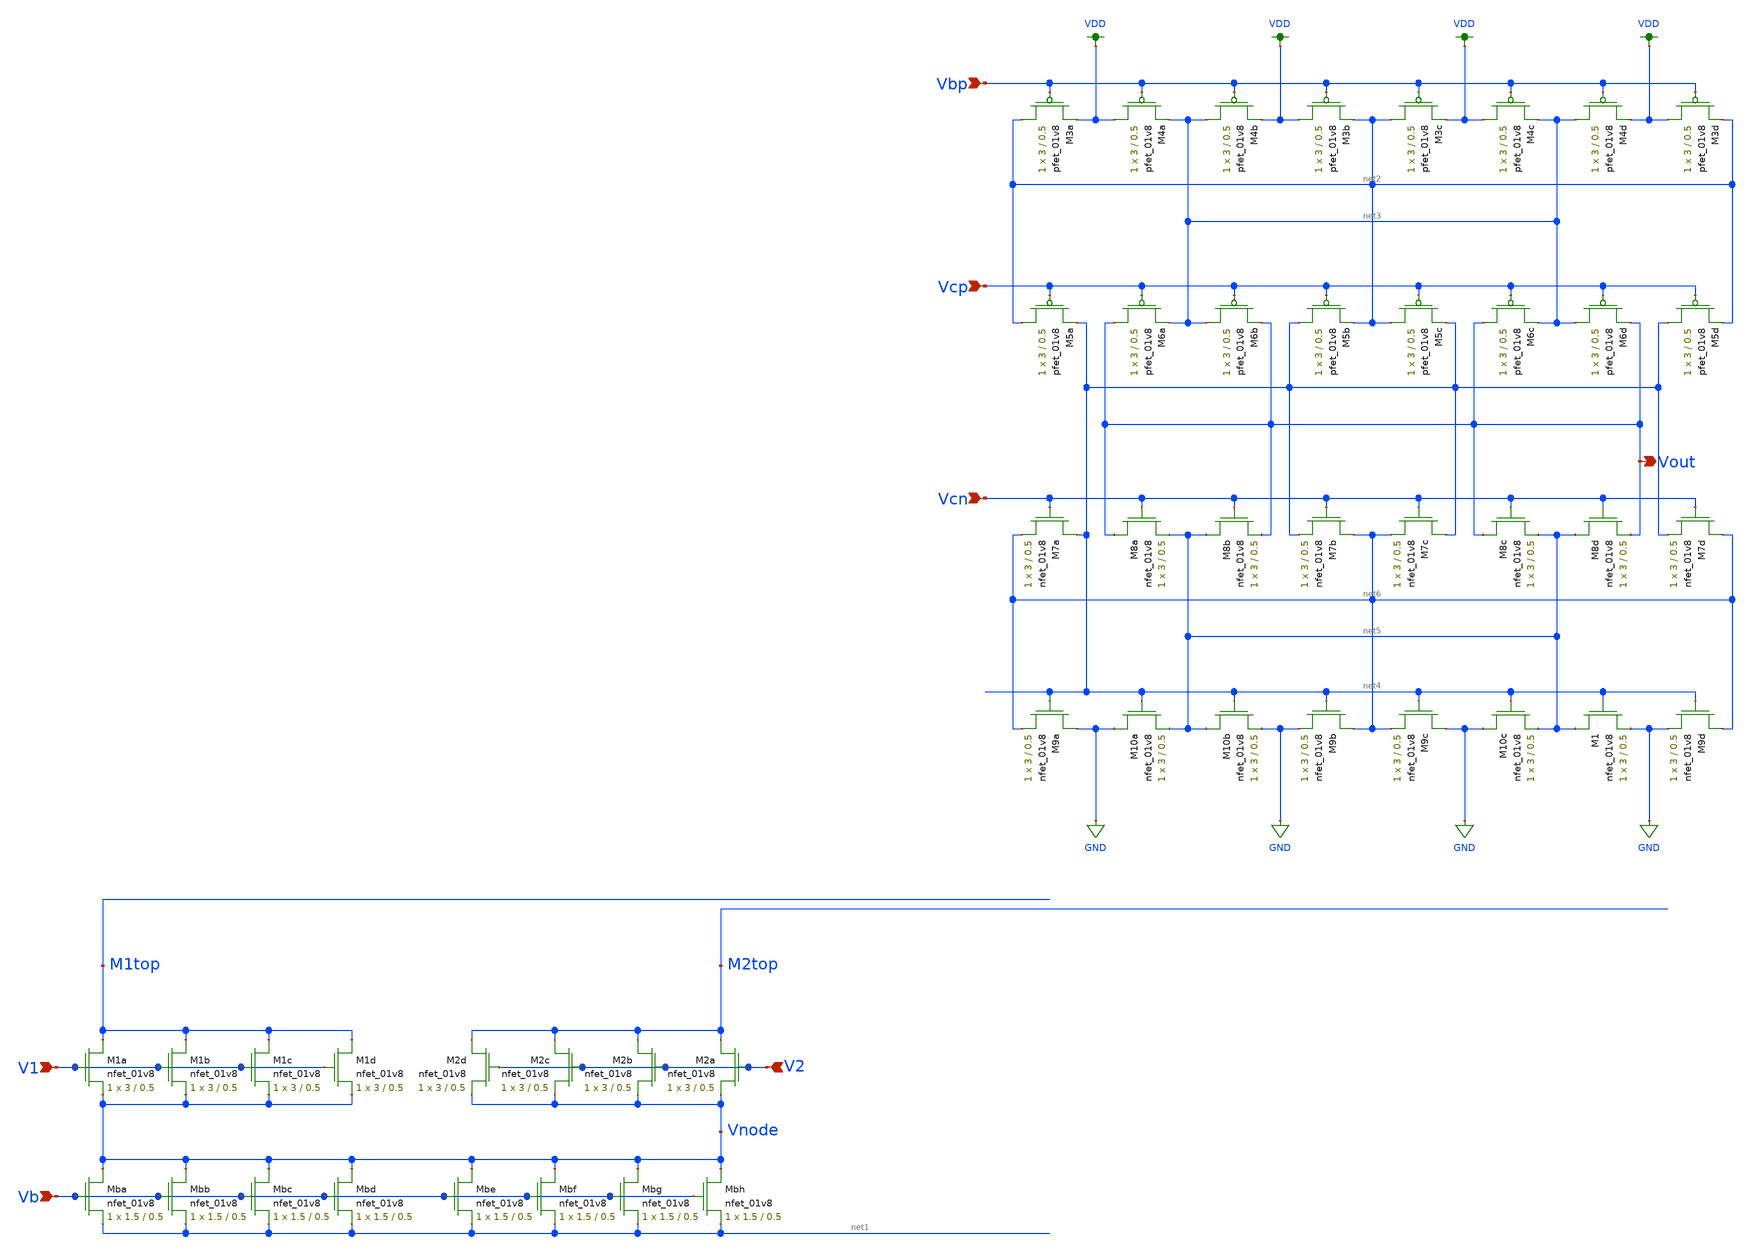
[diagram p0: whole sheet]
** sch_path: mp3/xschem/opamp_layout.sch
**.subckt opamp_layout Vbp Vcp Vcn V2 V1 Vb Vout
*.ipin Vbp
*.ipin Vcp
*.ipin Vcn
*.ipin V2
*.ipin V1
*.ipin Vb
*.opin Vout
XM1a M1top V1 Vnode GND sky130_fd_pr__nfet_01v8 L=0.5 W=3 nf=1 ad='int((nf+1)/2) * W/nf * 0.29' as='int((nf+2)/2) * W/nf * 0.29'
+ pd='2*int((nf+1)/2) * (W/nf + 0.29)' ps='2*int((nf+2)/2) * (W/nf + 0.29)' nrd='0.29 / W' nrs='0.29 / W'
+ sa=0 sb=0 sd=0 mult=1 m=1
XM1b M1top V1 Vnode GND sky130_fd_pr__nfet_01v8 L=0.5 W=3 nf=1 ad='int((nf+1)/2) * W/nf * 0.29' as='int((nf+2)/2) * W/nf * 0.29'
+ pd='2*int((nf+1)/2) * (W/nf + 0.29)' ps='2*int((nf+2)/2) * (W/nf + 0.29)' nrd='0.29 / W' nrs='0.29 / W'
+ sa=0 sb=0 sd=0 mult=1 m=1
XM1c M1top V1 Vnode GND sky130_fd_pr__nfet_01v8 L=0.5 W=3 nf=1 ad='int((nf+1)/2) * W/nf * 0.29' as='int((nf+2)/2) * W/nf * 0.29'
+ pd='2*int((nf+1)/2) * (W/nf + 0.29)' ps='2*int((nf+2)/2) * (W/nf + 0.29)' nrd='0.29 / W' nrs='0.29 / W'
+ sa=0 sb=0 sd=0 mult=1 m=1
XM1d M1top V1 Vnode GND sky130_fd_pr__nfet_01v8 L=0.5 W=3 nf=1 ad='int((nf+1)/2) * W/nf * 0.29' as='int((nf+2)/2) * W/nf * 0.29'
+ pd='2*int((nf+1)/2) * (W/nf + 0.29)' ps='2*int((nf+2)/2) * (W/nf + 0.29)' nrd='0.29 / W' nrs='0.29 / W'
+ sa=0 sb=0 sd=0 mult=1 m=1
XM2a M2top V2 Vnode GND sky130_fd_pr__nfet_01v8 L=0.5 W=3 nf=1 ad='int((nf+1)/2) * W/nf * 0.29' as='int((nf+2)/2) * W/nf * 0.29'
+ pd='2*int((nf+1)/2) * (W/nf + 0.29)' ps='2*int((nf+2)/2) * (W/nf + 0.29)' nrd='0.29 / W' nrs='0.29 / W'
+ sa=0 sb=0 sd=0 mult=1 m=1
XM2b M2top V2 Vnode GND sky130_fd_pr__nfet_01v8 L=0.5 W=3 nf=1 ad='int((nf+1)/2) * W/nf * 0.29' as='int((nf+2)/2) * W/nf * 0.29'
+ pd='2*int((nf+1)/2) * (W/nf + 0.29)' ps='2*int((nf+2)/2) * (W/nf + 0.29)' nrd='0.29 / W' nrs='0.29 / W'
+ sa=0 sb=0 sd=0 mult=1 m=1
XM2c M2top V2 Vnode GND sky130_fd_pr__nfet_01v8 L=0.5 W=3 nf=1 ad='int((nf+1)/2) * W/nf * 0.29' as='int((nf+2)/2) * W/nf * 0.29'
+ pd='2*int((nf+1)/2) * (W/nf + 0.29)' ps='2*int((nf+2)/2) * (W/nf + 0.29)' nrd='0.29 / W' nrs='0.29 / W'
+ sa=0 sb=0 sd=0 mult=1 m=1
XM2d M2top V2 Vnode GND sky130_fd_pr__nfet_01v8 L=0.5 W=3 nf=1 ad='int((nf+1)/2) * W/nf * 0.29' as='int((nf+2)/2) * W/nf * 0.29'
+ pd='2*int((nf+1)/2) * (W/nf + 0.29)' ps='2*int((nf+2)/2) * (W/nf + 0.29)' nrd='0.29 / W' nrs='0.29 / W'
+ sa=0 sb=0 sd=0 mult=1 m=1
XMba Vnode Vb net1 GND sky130_fd_pr__nfet_01v8 L=0.5 W=1.5 nf=1 ad='int((nf+1)/2) * W/nf * 0.29' as='int((nf+2)/2) * W/nf * 0.29'
+ pd='2*int((nf+1)/2) * (W/nf + 0.29)' ps='2*int((nf+2)/2) * (W/nf + 0.29)' nrd='0.29 / W' nrs='0.29 / W'
+ sa=0 sb=0 sd=0 mult=1 m=1
XMbb Vnode Vb net1 GND sky130_fd_pr__nfet_01v8 L=0.5 W=1.5 nf=1 ad='int((nf+1)/2) * W/nf * 0.29' as='int((nf+2)/2) * W/nf * 0.29'
+ pd='2*int((nf+1)/2) * (W/nf + 0.29)' ps='2*int((nf+2)/2) * (W/nf + 0.29)' nrd='0.29 / W' nrs='0.29 / W'
+ sa=0 sb=0 sd=0 mult=1 m=1
XMbc Vnode Vb net1 GND sky130_fd_pr__nfet_01v8 L=0.5 W=1.5 nf=1 ad='int((nf+1)/2) * W/nf * 0.29' as='int((nf+2)/2) * W/nf * 0.29'
+ pd='2*int((nf+1)/2) * (W/nf + 0.29)' ps='2*int((nf+2)/2) * (W/nf + 0.29)' nrd='0.29 / W' nrs='0.29 / W'
+ sa=0 sb=0 sd=0 mult=1 m=1
XMbd Vnode Vb net1 GND sky130_fd_pr__nfet_01v8 L=0.5 W=1.5 nf=1 ad='int((nf+1)/2) * W/nf * 0.29' as='int((nf+2)/2) * W/nf * 0.29'
+ pd='2*int((nf+1)/2) * (W/nf + 0.29)' ps='2*int((nf+2)/2) * (W/nf + 0.29)' nrd='0.29 / W' nrs='0.29 / W'
+ sa=0 sb=0 sd=0 mult=1 m=1
XMbe Vnode Vb net1 GND sky130_fd_pr__nfet_01v8 L=0.5 W=1.5 nf=1 ad='int((nf+1)/2) * W/nf * 0.29' as='int((nf+2)/2) * W/nf * 0.29'
+ pd='2*int((nf+1)/2) * (W/nf + 0.29)' ps='2*int((nf+2)/2) * (W/nf + 0.29)' nrd='0.29 / W' nrs='0.29 / W'
+ sa=0 sb=0 sd=0 mult=1 m=1
XMbf Vnode Vb net1 GND sky130_fd_pr__nfet_01v8 L=0.5 W=1.5 nf=1 ad='int((nf+1)/2) * W/nf * 0.29' as='int((nf+2)/2) * W/nf * 0.29'
+ pd='2*int((nf+1)/2) * (W/nf + 0.29)' ps='2*int((nf+2)/2) * (W/nf + 0.29)' nrd='0.29 / W' nrs='0.29 / W'
+ sa=0 sb=0 sd=0 mult=1 m=1
XMbg Vnode Vb net1 GND sky130_fd_pr__nfet_01v8 L=0.5 W=1.5 nf=1 ad='int((nf+1)/2) * W/nf * 0.29' as='int((nf+2)/2) * W/nf * 0.29'
+ pd='2*int((nf+1)/2) * (W/nf + 0.29)' ps='2*int((nf+2)/2) * (W/nf + 0.29)' nrd='0.29 / W' nrs='0.29 / W'
+ sa=0 sb=0 sd=0 mult=1 m=1
XMbh Vnode Vb net1 GND sky130_fd_pr__nfet_01v8 L=0.5 W=1.5 nf=1 ad='int((nf+1)/2) * W/nf * 0.29' as='int((nf+2)/2) * W/nf * 0.29'
+ pd='2*int((nf+1)/2) * (W/nf + 0.29)' ps='2*int((nf+2)/2) * (W/nf + 0.29)' nrd='0.29 / W' nrs='0.29 / W'
+ sa=0 sb=0 sd=0 mult=1 m=1
XM7a net4 Vcn net6 GND sky130_fd_pr__nfet_01v8 L=0.5 W=3 nf=1 ad='int((nf+1)/2) * W/nf * 0.29' as='int((nf+2)/2) * W/nf * 0.29'
+ pd='2*int((nf+1)/2) * (W/nf + 0.29)' ps='2*int((nf+2)/2) * (W/nf + 0.29)' nrd='0.29 / W' nrs='0.29 / W'
+ sa=0 sb=0 sd=0 mult=1 m=1
XM7b net6 Vcn net4 GND sky130_fd_pr__nfet_01v8 L=0.5 W=3 nf=1 ad='int((nf+1)/2) * W/nf * 0.29' as='int((nf+2)/2) * W/nf * 0.29'
+ pd='2*int((nf+1)/2) * (W/nf + 0.29)' ps='2*int((nf+2)/2) * (W/nf + 0.29)' nrd='0.29 / W' nrs='0.29 / W'
+ sa=0 sb=0 sd=0 mult=1 m=1
XM7c net4 Vcn net6 GND sky130_fd_pr__nfet_01v8 L=0.5 W=3 nf=1 ad='int((nf+1)/2) * W/nf * 0.29' as='int((nf+2)/2) * W/nf * 0.29'
+ pd='2*int((nf+1)/2) * (W/nf + 0.29)' ps='2*int((nf+2)/2) * (W/nf + 0.29)' nrd='0.29 / W' nrs='0.29 / W'
+ sa=0 sb=0 sd=0 mult=1 m=1
XM7d net6 Vcn net4 GND sky130_fd_pr__nfet_01v8 L=0.5 W=3 nf=1 ad='int((nf+1)/2) * W/nf * 0.29' as='int((nf+2)/2) * W/nf * 0.29'
+ pd='2*int((nf+1)/2) * (W/nf + 0.29)' ps='2*int((nf+2)/2) * (W/nf + 0.29)' nrd='0.29 / W' nrs='0.29 / W'
+ sa=0 sb=0 sd=0 mult=1 m=1
XM8a Vout Vcn net5 GND sky130_fd_pr__nfet_01v8 L=0.5 W=3 nf=1 ad='int((nf+1)/2) * W/nf * 0.29' as='int((nf+2)/2) * W/nf * 0.29'
+ pd='2*int((nf+1)/2) * (W/nf + 0.29)' ps='2*int((nf+2)/2) * (W/nf + 0.29)' nrd='0.29 / W' nrs='0.29 / W'
+ sa=0 sb=0 sd=0 mult=1 m=1
XM8b net5 Vcn Vout GND sky130_fd_pr__nfet_01v8 L=0.5 W=3 nf=1 ad='int((nf+1)/2) * W/nf * 0.29' as='int((nf+2)/2) * W/nf * 0.29'
+ pd='2*int((nf+1)/2) * (W/nf + 0.29)' ps='2*int((nf+2)/2) * (W/nf + 0.29)' nrd='0.29 / W' nrs='0.29 / W'
+ sa=0 sb=0 sd=0 mult=1 m=1
XM8c Vout Vcn net5 GND sky130_fd_pr__nfet_01v8 L=0.5 W=3 nf=1 ad='int((nf+1)/2) * W/nf * 0.29' as='int((nf+2)/2) * W/nf * 0.29'
+ pd='2*int((nf+1)/2) * (W/nf + 0.29)' ps='2*int((nf+2)/2) * (W/nf + 0.29)' nrd='0.29 / W' nrs='0.29 / W'
+ sa=0 sb=0 sd=0 mult=1 m=1
XM8d net5 Vcn Vout GND sky130_fd_pr__nfet_01v8 L=0.5 W=3 nf=1 ad='int((nf+1)/2) * W/nf * 0.29' as='int((nf+2)/2) * W/nf * 0.29'
+ pd='2*int((nf+1)/2) * (W/nf + 0.29)' ps='2*int((nf+2)/2) * (W/nf + 0.29)' nrd='0.29 / W' nrs='0.29 / W'
+ sa=0 sb=0 sd=0 mult=1 m=1
XM9a GND net4 net6 GND sky130_fd_pr__nfet_01v8 L=0.5 W=3 nf=1 ad='int((nf+1)/2) * W/nf * 0.29' as='int((nf+2)/2) * W/nf * 0.29'
+ pd='2*int((nf+1)/2) * (W/nf + 0.29)' ps='2*int((nf+2)/2) * (W/nf + 0.29)' nrd='0.29 / W' nrs='0.29 / W'
+ sa=0 sb=0 sd=0 mult=1 m=1
XM9b net6 net4 GND GND sky130_fd_pr__nfet_01v8 L=0.5 W=3 nf=1 ad='int((nf+1)/2) * W/nf * 0.29' as='int((nf+2)/2) * W/nf * 0.29'
+ pd='2*int((nf+1)/2) * (W/nf + 0.29)' ps='2*int((nf+2)/2) * (W/nf + 0.29)' nrd='0.29 / W' nrs='0.29 / W'
+ sa=0 sb=0 sd=0 mult=1 m=1
XM9c GND net4 net6 GND sky130_fd_pr__nfet_01v8 L=0.5 W=3 nf=1 ad='int((nf+1)/2) * W/nf * 0.29' as='int((nf+2)/2) * W/nf * 0.29'
+ pd='2*int((nf+1)/2) * (W/nf + 0.29)' ps='2*int((nf+2)/2) * (W/nf + 0.29)' nrd='0.29 / W' nrs='0.29 / W'
+ sa=0 sb=0 sd=0 mult=1 m=1
XM9d net6 net4 GND GND sky130_fd_pr__nfet_01v8 L=0.5 W=3 nf=1 ad='int((nf+1)/2) * W/nf * 0.29' as='int((nf+2)/2) * W/nf * 0.29'
+ pd='2*int((nf+1)/2) * (W/nf + 0.29)' ps='2*int((nf+2)/2) * (W/nf + 0.29)' nrd='0.29 / W' nrs='0.29 / W'
+ sa=0 sb=0 sd=0 mult=1 m=1
XM10a GND net4 net5 GND sky130_fd_pr__nfet_01v8 L=0.5 W=3 nf=1 ad='int((nf+1)/2) * W/nf * 0.29' as='int((nf+2)/2) * W/nf * 0.29'
+ pd='2*int((nf+1)/2) * (W/nf + 0.29)' ps='2*int((nf+2)/2) * (W/nf + 0.29)' nrd='0.29 / W' nrs='0.29 / W'
+ sa=0 sb=0 sd=0 mult=1 m=1
XM10b net5 net4 GND GND sky130_fd_pr__nfet_01v8 L=0.5 W=3 nf=1 ad='int((nf+1)/2) * W/nf * 0.29' as='int((nf+2)/2) * W/nf * 0.29'
+ pd='2*int((nf+1)/2) * (W/nf + 0.29)' ps='2*int((nf+2)/2) * (W/nf + 0.29)' nrd='0.29 / W' nrs='0.29 / W'
+ sa=0 sb=0 sd=0 mult=1 m=1
XM10c GND net4 net5 GND sky130_fd_pr__nfet_01v8 L=0.5 W=3 nf=1 ad='int((nf+1)/2) * W/nf * 0.29' as='int((nf+2)/2) * W/nf * 0.29'
+ pd='2*int((nf+1)/2) * (W/nf + 0.29)' ps='2*int((nf+2)/2) * (W/nf + 0.29)' nrd='0.29 / W' nrs='0.29 / W'
+ sa=0 sb=0 sd=0 mult=1 m=1
XM1 net5 net4 GND GND sky130_fd_pr__nfet_01v8 L=0.5 W=3 nf=1 ad='int((nf+1)/2) * W/nf * 0.29' as='int((nf+2)/2) * W/nf * 0.29'
+ pd='2*int((nf+1)/2) * (W/nf + 0.29)' ps='2*int((nf+2)/2) * (W/nf + 0.29)' nrd='0.29 / W' nrs='0.29 / W'
+ sa=0 sb=0 sd=0 mult=1 m=1
XM5a net2 Vcp net4 VDD sky130_fd_pr__pfet_01v8 L=0.5 W=3 nf=1 ad='int((nf+1)/2) * W/nf * 0.29' as='int((nf+2)/2) * W/nf * 0.29'
+ pd='2*int((nf+1)/2) * (W/nf + 0.29)' ps='2*int((nf+2)/2) * (W/nf + 0.29)' nrd='0.29 / W' nrs='0.29 / W'
+ sa=0 sb=0 sd=0 mult=1 m=1
XM5b net4 Vcp net2 VDD sky130_fd_pr__pfet_01v8 L=0.5 W=3 nf=1 ad='int((nf+1)/2) * W/nf * 0.29' as='int((nf+2)/2) * W/nf * 0.29'
+ pd='2*int((nf+1)/2) * (W/nf + 0.29)' ps='2*int((nf+2)/2) * (W/nf + 0.29)' nrd='0.29 / W' nrs='0.29 / W'
+ sa=0 sb=0 sd=0 mult=1 m=1
XM5c net2 Vcp net4 VDD sky130_fd_pr__pfet_01v8 L=0.5 W=3 nf=1 ad='int((nf+1)/2) * W/nf * 0.29' as='int((nf+2)/2) * W/nf * 0.29'
+ pd='2*int((nf+1)/2) * (W/nf + 0.29)' ps='2*int((nf+2)/2) * (W/nf + 0.29)' nrd='0.29 / W' nrs='0.29 / W'
+ sa=0 sb=0 sd=0 mult=1 m=1
XM5d net4 Vcp net2 VDD sky130_fd_pr__pfet_01v8 L=0.5 W=3 nf=1 ad='int((nf+1)/2) * W/nf * 0.29' as='int((nf+2)/2) * W/nf * 0.29'
+ pd='2*int((nf+1)/2) * (W/nf + 0.29)' ps='2*int((nf+2)/2) * (W/nf + 0.29)' nrd='0.29 / W' nrs='0.29 / W'
+ sa=0 sb=0 sd=0 mult=1 m=1
XM6a Vout Vcp net3 VDD sky130_fd_pr__pfet_01v8 L=0.5 W=3 nf=1 ad='int((nf+1)/2) * W/nf * 0.29' as='int((nf+2)/2) * W/nf * 0.29'
+ pd='2*int((nf+1)/2) * (W/nf + 0.29)' ps='2*int((nf+2)/2) * (W/nf + 0.29)' nrd='0.29 / W' nrs='0.29 / W'
+ sa=0 sb=0 sd=0 mult=1 m=1
XM6b net3 Vcp Vout VDD sky130_fd_pr__pfet_01v8 L=0.5 W=3 nf=1 ad='int((nf+1)/2) * W/nf * 0.29' as='int((nf+2)/2) * W/nf * 0.29'
+ pd='2*int((nf+1)/2) * (W/nf + 0.29)' ps='2*int((nf+2)/2) * (W/nf + 0.29)' nrd='0.29 / W' nrs='0.29 / W'
+ sa=0 sb=0 sd=0 mult=1 m=1
XM6c Vout Vcp net3 VDD sky130_fd_pr__pfet_01v8 L=0.5 W=3 nf=1 ad='int((nf+1)/2) * W/nf * 0.29' as='int((nf+2)/2) * W/nf * 0.29'
+ pd='2*int((nf+1)/2) * (W/nf + 0.29)' ps='2*int((nf+2)/2) * (W/nf + 0.29)' nrd='0.29 / W' nrs='0.29 / W'
+ sa=0 sb=0 sd=0 mult=1 m=1
XM6d net3 Vcp Vout VDD sky130_fd_pr__pfet_01v8 L=0.5 W=3 nf=1 ad='int((nf+1)/2) * W/nf * 0.29' as='int((nf+2)/2) * W/nf * 0.29'
+ pd='2*int((nf+1)/2) * (W/nf + 0.29)' ps='2*int((nf+2)/2) * (W/nf + 0.29)' nrd='0.29 / W' nrs='0.29 / W'
+ sa=0 sb=0 sd=0 mult=1 m=1
XM3a net2 Vbp VDD VDD sky130_fd_pr__pfet_01v8 L=0.5 W=3 nf=1 ad='int((nf+1)/2) * W/nf * 0.29' as='int((nf+2)/2) * W/nf * 0.29'
+ pd='2*int((nf+1)/2) * (W/nf + 0.29)' ps='2*int((nf+2)/2) * (W/nf + 0.29)' nrd='0.29 / W' nrs='0.29 / W'
+ sa=0 sb=0 sd=0 mult=1 m=1
XM3b VDD Vbp net2 VDD sky130_fd_pr__pfet_01v8 L=0.5 W=3 nf=1 ad='int((nf+1)/2) * W/nf * 0.29' as='int((nf+2)/2) * W/nf * 0.29'
+ pd='2*int((nf+1)/2) * (W/nf + 0.29)' ps='2*int((nf+2)/2) * (W/nf + 0.29)' nrd='0.29 / W' nrs='0.29 / W'
+ sa=0 sb=0 sd=0 mult=1 m=1
XM3c net2 Vbp VDD VDD sky130_fd_pr__pfet_01v8 L=0.5 W=3 nf=1 ad='int((nf+1)/2) * W/nf * 0.29' as='int((nf+2)/2) * W/nf * 0.29'
+ pd='2*int((nf+1)/2) * (W/nf + 0.29)' ps='2*int((nf+2)/2) * (W/nf + 0.29)' nrd='0.29 / W' nrs='0.29 / W'
+ sa=0 sb=0 sd=0 mult=1 m=1
XM3d VDD Vbp net2 VDD sky130_fd_pr__pfet_01v8 L=0.5 W=3 nf=1 ad='int((nf+1)/2) * W/nf * 0.29' as='int((nf+2)/2) * W/nf * 0.29'
+ pd='2*int((nf+1)/2) * (W/nf + 0.29)' ps='2*int((nf+2)/2) * (W/nf + 0.29)' nrd='0.29 / W' nrs='0.29 / W'
+ sa=0 sb=0 sd=0 mult=1 m=1
XM4a VDD Vbp net3 VDD sky130_fd_pr__pfet_01v8 L=0.5 W=3 nf=1 ad='int((nf+1)/2) * W/nf * 0.29' as='int((nf+2)/2) * W/nf * 0.29'
+ pd='2*int((nf+1)/2) * (W/nf + 0.29)' ps='2*int((nf+2)/2) * (W/nf + 0.29)' nrd='0.29 / W' nrs='0.29 / W'
+ sa=0 sb=0 sd=0 mult=1 m=1
XM4b net3 Vbp VDD VDD sky130_fd_pr__pfet_01v8 L=0.5 W=3 nf=1 ad='int((nf+1)/2) * W/nf * 0.29' as='int((nf+2)/2) * W/nf * 0.29'
+ pd='2*int((nf+1)/2) * (W/nf + 0.29)' ps='2*int((nf+2)/2) * (W/nf + 0.29)' nrd='0.29 / W' nrs='0.29 / W'
+ sa=0 sb=0 sd=0 mult=1 m=1
XM4c VDD Vbp net3 VDD sky130_fd_pr__pfet_01v8 L=0.5 W=3 nf=1 ad='int((nf+1)/2) * W/nf * 0.29' as='int((nf+2)/2) * W/nf * 0.29'
+ pd='2*int((nf+1)/2) * (W/nf + 0.29)' ps='2*int((nf+2)/2) * (W/nf + 0.29)' nrd='0.29 / W' nrs='0.29 / W'
+ sa=0 sb=0 sd=0 mult=1 m=1
XM4d net3 Vbp VDD VDD sky130_fd_pr__pfet_01v8 L=0.5 W=3 nf=1 ad='int((nf+1)/2) * W/nf * 0.29' as='int((nf+2)/2) * W/nf * 0.29'
+ pd='2*int((nf+1)/2) * (W/nf + 0.29)' ps='2*int((nf+2)/2) * (W/nf + 0.29)' nrd='0.29 / W' nrs='0.29 / W'
+ sa=0 sb=0 sd=0 mult=1 m=1
**.ends
.GLOBAL VDD
.GLOBAL GND
.end
